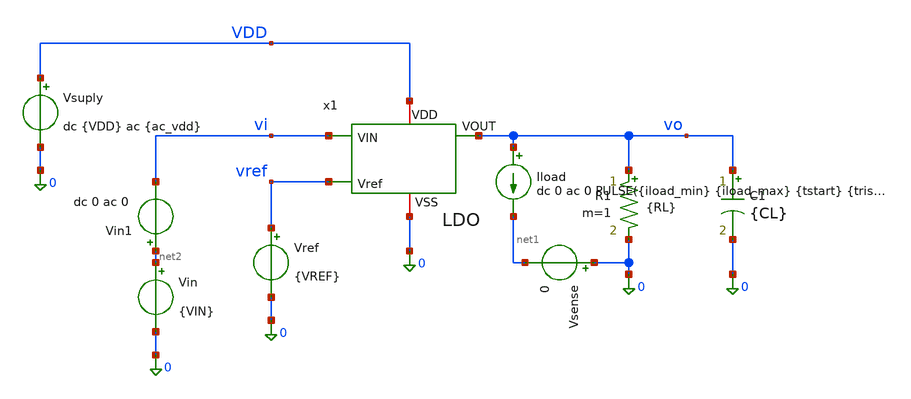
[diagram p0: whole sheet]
** sch_path: xschem/ldo_tb_montecarlo.sch
**.subckt ldo_tb_montecarlo
Vsuply VDD 0 dc {VDD} ac {ac_vdd}
Vref vref 0 {VREF}
Vin net2 0 {VIN}
R1 vo 0 {RL} m=1
C1 vo 0 {CL} m=1
Iload vo net1 dc 0 ac 0 PULSE({iload_min} {iload_max} {tstart} {trise} {tfall} {twidth} {tperiod})
Vsense 0 net1 0
Vin1 net2 vi dc 0 ac 0
x1 vi vo VDD vref 0 LDO
**** begin user architecture code




.lib /foss/pdks/sky130A/libs.tech/ngspice/sky130.lib.spice tt_mm

.option temp=125
.option num_threads=8

**parametros_ldo
.param VDD = 1.8
.param VREF = 0.6
.param VIN = '1*VDD'
.param RL = 24
.param CL = 1u

* Parámetros para la prueba de carga del LDO
.param iload_min = 1m
.param iload_max = 50m
.param tstart   = 10u
.param trise    = 100n
.param tfall    = 100n
.param twidth   = 200u
.param tperiod  = 400u
.param tsim = '5*tperiod'

.param ac_iprobe = 1
.param ac_vdd = 0

.control
* =========================================================
* 1. CONFIGURACIÓN DEL BUCLE MONTE CARLO
* =========================================================
let mc_runs = 100
let run = 1

set appendwrite
set filetype=ascii

* En .control 'let' NO acepta comillas: se evalua directamente la expresion
let tperiod  = 400u
let tsim = 5*tperiod

* ---> CREAR EL ARCHIVO LIMPIO ANTES DEL BUCLE <---
* El símbolo '>' crea un archivo nuevo o borra el anterior si existía
echo === INICIO MONTE CARLO === > datos_mc.txt

* =========================================================
* 2. INICIO DEL BUCLE
* =========================================================
while run <= mc_runs
    alterparam ac_iprobe = 1
    alterparam ac_vdd = 0
    alterparam RL = 24

    * Mensajes en la consola de Ngspice para que veas el progreso visual
    echo ======================================
    echo CORRIENDO MONTE CARLO ITERACION: $&run
    echo ======================================

    * Guardamos un separador de iteración en el archivo de texto
    echo --- ITERACION: $&run --- >> datos_mc.txt

    * Tira los dados estadísticos para crear un nuevo chip
    reset

    * -----------------------------------------------------
    * B. TRANSIENTE (Overshoot y Undershoot)
    * -----------------------------------------------------
    tran 1u $&tsim
    write LDO_mc_tran.raw

    meas tran v_estable_ligera FIND v(vo) AT=9u
    meas tran v_estable_pesada FIND v(vo) AT=209u
    meas tran vo_max MAX v(vo)
    meas tran vo_min MIN v(vo)

    let undershoot_mV = (v_estable_ligera - vo_min) * 1e3
    let overshoot_mV = (vo_max - v_estable_pesada) * 1e3

    * Escribimos los datos en el archivo .txt usando '>>'
    echo 'undershoot_mV = $&undershoot_mV' >> datos_mc.txt
    echo 'overshoot_mV = $&overshoot_mV' >> datos_mc.txt

    * -----------------------------------------------------
    * C. AC (Estabilidad y Ganancia de Lazo Abierto)
    * -----------------------------------------------------
    ac dec 10 1 1G
    * 1. Ganancia de Lazo Abierto T(s) = v(x1.vre) / v(x1.vre2)
    let T_loop = v(x1.vre) / v(x1.vre2)
    let ldb = vdb(T_loop)
    let fase = vp(T_loop) * 180 / pi

    write LDO_mc_ac_estability.raw

    meas ac ugb WHEN ldb = 0.0
    meas ac fase_ugb FIND fase WHEN ldb = 0.0
    let margen_fase = fase_ugb
    meas ac ganancia_banda_plana find ldb at=1

    echo 'margen_fase = $&margen_fase' >> datos_mc.txt
    echo 'ganancia_banda_plana = $&ganancia_banda_plana' >> datos_mc.txt
    echo 'ugb = $&ugb' >> datos_mc.txt

    * -----------------------------------------------------
    * D. DC (Line Regulation)
    * -----------------------------------------------------
    dc vin 1.3 2 0.01
    write LDO_mc_dc_line.raw

    meas dc voline_max MAX v(vo)
    meas dc voline_min MIN v(vo)
    let line_regulation = (voline_max - voline_min)*1000

    echo 'line_regulation = $&line_regulation' >> datos_mc.txt

    * -----------------------------------------------------
    * E. AC (PSRR)
    * -----------------------------------------------------
    alterparam ac_iprobe = 0
    alterparam ac_vdd = 1
    reset
    ac dec 10 1 1G
    let psrr1 = v(vdd)/v(vo)
    let psrr_db = vdb(psrr1)
    write LDO_mc_ac_psrr.raw

    meas ac gananciaPSRR_1   find psrr_db at=1
    meas ac gananciaPSRR_1k  find psrr_db at=1k
    meas ac gananciaPSRR_10k find psrr_db at=10k
    meas ac gananciaPSRR_1M  find psrr_db at=1Meg

    echo 'psrr_1 = $&gananciaPSRR_1' >> datos_mc.txt
    echo 'psrr_1k = $&gananciaPSRR_1k' >> datos_mc.txt
    echo 'psrr_10k = $&gananciaPSRR_10k' >> datos_mc.txt
    echo 'psrr_1M = $&gananciaPSRR_1M' >> datos_mc.txt

    * -----------------------------------------------------
    * F. DC (Load Regulation)
    * -----------------------------------------------------
    alterparam RL = 1e9
    reset
    dc iload 400u 50m 100u
    write LDO_mc_dc_load.raw

    meas dc voload_max MAX v(vo)
    meas dc voload_min MIN v(vo)
    let load_regulation = (voload_max - voload_min)*1000

    echo 'load_regulation = $&load_regulation' >> datos_mc.txt

    * -----------------------------------------------------
    * G. DC (Dropout)
    * -----------------------------------------------------
    alterparam RL = 24
    reset
    dc vin1 0 2 0.01
    write LDO_mc_dc_dropout.raw

    meas dc vout_nom FIND v(vo) WHEN vi = 1.55
    let vout_target = vout_nom * 0.995
    meas dc vin_do FIND vi WHEN vo = vout_target fall=1
    let dropout_mV = (vin_do - vout_target) * 1e3

    echo 'dropout_mV = $&dropout_mV' >> datos_mc.txt

    * Avanzamos el contador del bucle
    let run = run + 1
end

* Al terminar, imprimimos que finalizó
echo ======================================
echo SIMULACION MONTE CARLO FINALIZADA
echo ======================================
echo === FIN MONTE CARLO === >> datos_mc.txt

.endc



**** end user architecture code
**.ends

* expanding   symbol:  /foss/designs/LDO-sky130/xschem/LDO.sym # of pins=5
** sym_path: xschem/LDO.sym
** sch_path: xschem/LDO.sch
.subckt LDO VIN VOUT VDD Vref VSS
*.ipin VIN
*.iopin VDD
*.opin VOUT
*.ipin Vref
*.iopin VSS
XR1 Vre VOUT VSS sky130_fd_pr__res_iso_pw W=0.35 L=10.17 m=1
XR2 VSS Vre VSS sky130_fd_pr__res_iso_pw W=0.35 L=10 m=1
V1 vre2 Vre 0 ac {ac_iprobe}
XC1 VOUT Vre sky130_fd_pr__cap_mim_m3_2 W=19.5 L=19.5 MF=1 m=1
XC2 VOUT VSS sky130_fd_pr__cap_mim_m3_2 W=40 L=40 MF=1 m=1
x1 VDD Vgp Vref vre2 VSS OTA
XM2 VOUT Vgp VIN VDD sky130_fd_pr__pfet_01v8 L=0.5 W=1000 nf=100 ad='int((100 + 1)/2) * 1000 / 100 * 0.29'
+ as='int((100 + 2)/2) * 1000 / 100 * 0.29' pd='2*int((100 + 1)/2) * (1000 / 100 + 0.29)' ps='2*int((100 + 2)/2) * (1000 / 100 + 0.29)'
+ nrd='0.29 / 1000 ' nrs='0.29 / 1000 ' sa=0 sb=0 sd=0 mult=5 m=5
.ends


* expanding   symbol:  /foss/designs/LDO-sky130/xschem/OTA.sym # of pins=5
** sym_path: xschem/OTA.sym
** sch_path: xschem/OTA.sch
.subckt OTA VDD VO_ota VIN_ota VIP_ota VSS
*.ipin VIN_ota
*.opin VO_ota
*.iopin VSS
*.iopin VDD
*.ipin VIP_ota
XR1 VO_ota1 net1 VDD sky130_fd_pr__res_high_po W=0.35 L=360 mult=1 m=1
XC1 VO_ota net1 sky130_fd_pr__cap_mim_m3_2 W=50 L=50 MF=1 m=1
XMpr VO_ota1 vd VSS VSS sky130_fd_pr__nfet_01v8 L=0.5 W=3 nf=1 ad='int((1 + 1)/2) * 3 / 1 * 0.29' as='int((1 + 2)/2) * 3 / 1 * 0.29'
+ pd='2*int((1 + 1)/2) * (3 / 1 + 0.29)' ps='2*int((1 + 2)/2) * (3 / 1 + 0.29)' nrd='0.29 / 3 ' nrs='0.29 / 3 '
+ sa=0 sb=0 sd=0 mult=1 m=1
XMnr vd vd VSS VSS sky130_fd_pr__nfet_01v8 L=0.5 W=3 nf=1 ad='int((1 + 1)/2) * 3 / 1 * 0.29' as='int((1 + 2)/2) * 3 / 1 * 0.29'
+ pd='2*int((1 + 1)/2) * (3 / 1 + 0.29)' ps='2*int((1 + 2)/2) * (3 / 1 + 0.29)' nrd='0.29 / 3 ' nrs='0.29 / 3 '
+ sa=0 sb=0 sd=0 mult=1 m=1
XMn vd VIN_ota Vtail VDD sky130_fd_pr__pfet_01v8 L=0.5 W=28 nf=1 ad='int((1 + 1)/2) * 28 / 1 * 0.29'
+ as='int((1 + 2)/2) * 28 / 1 * 0.29' pd='2*int((1 + 1)/2) * (28 / 1 + 0.29)' ps='2*int((1 + 2)/2) * (28 / 1 + 0.29)'
+ nrd='0.29 / 28 ' nrs='0.29 / 28 ' sa=0 sb=0 sd=0 mult=1 m=1
XMp VO_ota1 VIP_ota Vtail VDD sky130_fd_pr__pfet_01v8 L=0.5 W=28 nf=1 ad='int((1 + 1)/2) * 28 / 1 * 0.29'
+ as='int((1 + 2)/2) * 28 / 1 * 0.29' pd='2*int((1 + 1)/2) * (28 / 1 + 0.29)' ps='2*int((1 + 2)/2) * (28 / 1 + 0.29)'
+ nrd='0.29 / 28 ' nrs='0.29 / 28 ' sa=0 sb=0 sd=0 mult=1 m=1
XMo VO_ota VO_ota1 VSS VSS sky130_fd_pr__nfet_01v8 L=0.5 W=3 nf=1 ad='int((1 + 1)/2) * 3 / 1 * 0.29'
+ as='int((1 + 2)/2) * 3 / 1 * 0.29' pd='2*int((1 + 1)/2) * (3 / 1 + 0.29)' ps='2*int((1 + 2)/2) * (3 / 1 + 0.29)'
+ nrd='0.29 / 3 ' nrs='0.29 / 3 ' sa=0 sb=0 sd=0 mult=1 m=1
XMrc1 Vtail VGP VDD VDD sky130_fd_pr__pfet_01v8_lvt L=0.5 W=40 nf=1 ad='int((1 + 1)/2) * 40 / 1 * 0.29'
+ as='int((1 + 2)/2) * 40 / 1 * 0.29' pd='2*int((1 + 1)/2) * (40 / 1 + 0.29)' ps='2*int((1 + 2)/2) * (40 / 1 + 0.29)'
+ nrd='0.29 / 40 ' nrs='0.29 / 40 ' sa=0 sb=0 sd=0 mult=1 m=1
XMrc2 VO_ota VGP VDD VDD sky130_fd_pr__pfet_01v8_lvt L=0.5 W=8 nf=1 ad='int((1 + 1)/2) * 8 / 1 * 0.29'
+ as='int((1 + 2)/2) * 8 / 1 * 0.29' pd='2*int((1 + 1)/2) * (8 / 1 + 0.29)' ps='2*int((1 + 2)/2) * (8 / 1 + 0.29)'
+ nrd='0.29 / 8 ' nrs='0.29 / 8 ' sa=0 sb=0 sd=0 mult=1 m=1
XMc3 VGP Viref rs VSS sky130_fd_pr__nfet_01v8 L=1 W=20 nf=1 ad='int((1 + 1)/2) * 20 / 1 * 0.29' as='int((1 + 2)/2) * 20 / 1 * 0.29'
+ pd='2*int((1 + 1)/2) * (20 / 1 + 0.29)' ps='2*int((1 + 2)/2) * (20 / 1 + 0.29)' nrd='0.29 / 20 ' nrs='0.29 / 20 '
+ sa=0 sb=0 sd=0 mult=1 m=1
XMp2 Viref Viref VSS VSS sky130_fd_pr__nfet_01v8 L=1 W=5 nf=1 ad='int((1 + 1)/2) * 5 / 1 * 0.29' as='int((1 + 2)/2) * 5 / 1 * 0.29'
+ pd='2*int((1 + 1)/2) * (5 / 1 + 0.29)' ps='2*int((1 + 2)/2) * (5 / 1 + 0.29)' nrd='0.29 / 5 ' nrs='0.29 / 5 '
+ sa=0 sb=0 sd=0 mult=1 m=1
XMr VGP VGP VDD VDD sky130_fd_pr__pfet_01v8_lvt L=0.5 W=2.4 nf=1 ad='int((1 + 1)/2) * 2.4 / 1 * 0.29'
+ as='int((1 + 2)/2) * 2.4 / 1 * 0.29' pd='2*int((1 + 1)/2) * (2.4 / 1 + 0.29)' ps='2*int((1 + 2)/2) * (2.4 / 1 + 0.29)'
+ nrd='0.29 / 2.4 ' nrs='0.29 / 2.4 ' sa=0 sb=0 sd=0 mult=1 m=1
XMr1 Viref VGP VDD VDD sky130_fd_pr__pfet_01v8_lvt L=1 W=8 nf=1 ad='int((1 + 1)/2) * 8 / 1 * 0.29' as='int((1 + 2)/2) * 8 / 1 * 0.29'
+ pd='2*int((1 + 1)/2) * (8 / 1 + 0.29)' ps='2*int((1 + 2)/2) * (8 / 1 + 0.29)' nrd='0.29 / 8 ' nrs='0.29 / 8 '
+ sa=0 sb=0 sd=0 mult=1 m=1
XRs VSS rs VSS sky130_fd_pr__res_iso_pw W=0.425 L=0.35 m=1
.ends

.end
